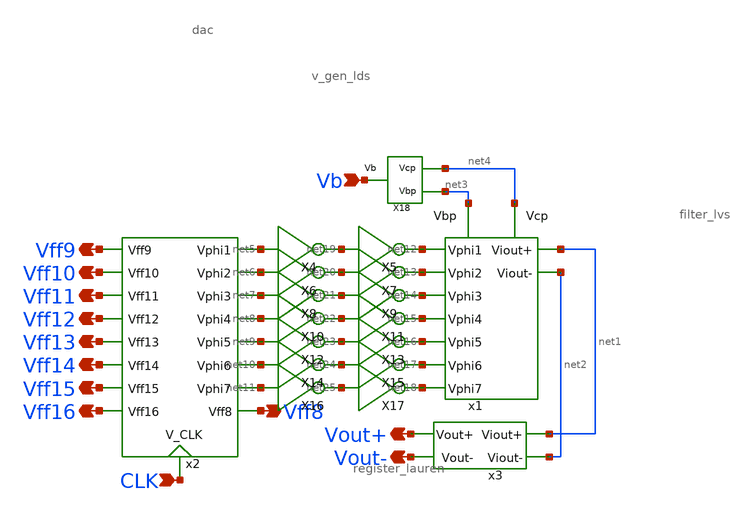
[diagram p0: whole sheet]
** sch_path: simulation/final_lds.sch
**.subckt final_lds Vb Vff9 Vff10 Vff11 Vff12 Vff13 Vff14 Vff15 Vff16 CLK Vff8 Vout+ Vout-
*.ipin Vb
*.opin Vff9
*.opin Vff10
*.opin Vff11
*.opin Vff12
*.opin Vff13
*.opin Vff14
*.opin Vff15
*.opin Vff16
*.ipin CLK
*.opin Vff8
*.opin Vout+
*.opin Vout-
x2 Vff10 Vff11 Vff12 Vff13 Vff14 Vff16 Vff15 Vff9 net5 net6 net7 net8 net9 net10 net11 Vff8 CLK
+ register_lauren
X18 net4 net3 Vb v_gen_lds
x1 net12 net13 net14 net15 net16 net17 net18 net1 net2 net3 net4 dac
X4 net5 net19 inverter
X5 net19 net12 inverter
X6 net6 net20 inverter
X7 net20 net13 inverter
X8 net7 net21 inverter
X9 net21 net14 inverter
X10 net8 net22 inverter
X11 net22 net15 inverter
X12 net9 net23 inverter
X13 net23 net16 inverter
X14 net10 net24 inverter
X15 net24 net17 inverter
X16 net11 net25 inverter
X17 net25 net18 inverter
x3 net1 net2 Vout+ Vout- filter_lvs
**.ends
.end
